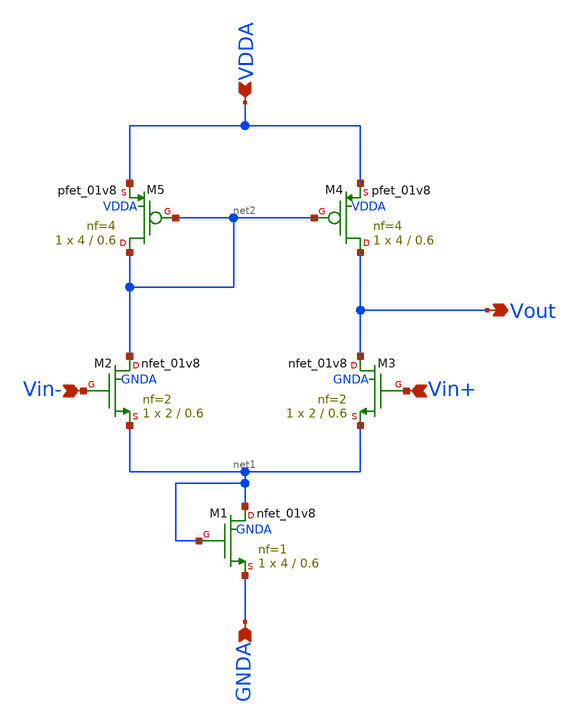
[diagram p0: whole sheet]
** sch_path: projects/bandgapref/xschem_ngspice/old_files/opamp_bandgap2.sch
**.subckt opamp_bandgap2 Vin+ Vout Vin- GNDA VDDA
*.ipin Vin+
*.opin Vout
*.ipin Vin-
*.ipin GNDA
*.ipin VDDA
XM2 net2 Vin- net1 GNDA sky130_fd_pr__nfet_01v8 L=0.6 W=2 nf=2 ad='int((nf+1)/2) * W/nf * 0.29' as='int((nf+2)/2) * W/nf * 0.29'
+ pd='2*int((nf+1)/2) * (W/nf + 0.29)' ps='2*int((nf+2)/2) * (W/nf + 0.29)' nrd='0.29 / W' nrs='0.29 / W'
+ sa=0 sb=0 sd=0 mult=1 m=1
XM3 Vout Vin+ net1 GNDA sky130_fd_pr__nfet_01v8 L=0.6 W=2 nf=2 ad='int((nf+1)/2) * W/nf * 0.29' as='int((nf+2)/2) * W/nf * 0.29'
+ pd='2*int((nf+1)/2) * (W/nf + 0.29)' ps='2*int((nf+2)/2) * (W/nf + 0.29)' nrd='0.29 / W' nrs='0.29 / W'
+ sa=0 sb=0 sd=0 mult=1 m=1
XM1 net1 net1 GNDA GNDA sky130_fd_pr__nfet_01v8 L=0.6 W=4 nf=1 ad='int((nf+1)/2) * W/nf * 0.29' as='int((nf+2)/2) * W/nf * 0.29'
+ pd='2*int((nf+1)/2) * (W/nf + 0.29)' ps='2*int((nf+2)/2) * (W/nf + 0.29)' nrd='0.29 / W' nrs='0.29 / W'
+ sa=0 sb=0 sd=0 mult=1 m=1
XM4 Vout net2 VDDA VDDA sky130_fd_pr__pfet_01v8 L=0.6 W=4 nf=4 ad='int((nf+1)/2) * W/nf * 0.29' as='int((nf+2)/2) * W/nf * 0.29'
+ pd='2*int((nf+1)/2) * (W/nf + 0.29)' ps='2*int((nf+2)/2) * (W/nf + 0.29)' nrd='0.29 / W' nrs='0.29 / W'
+ sa=0 sb=0 sd=0 mult=1 m=1
XM5 net2 net2 VDDA VDDA sky130_fd_pr__pfet_01v8 L=0.6 W=4 nf=4 ad='int((nf+1)/2) * W/nf * 0.29' as='int((nf+2)/2) * W/nf * 0.29'
+ pd='2*int((nf+1)/2) * (W/nf + 0.29)' ps='2*int((nf+2)/2) * (W/nf + 0.29)' nrd='0.29 / W' nrs='0.29 / W'
+ sa=0 sb=0 sd=0 mult=1 m=1
**.ends
.end
